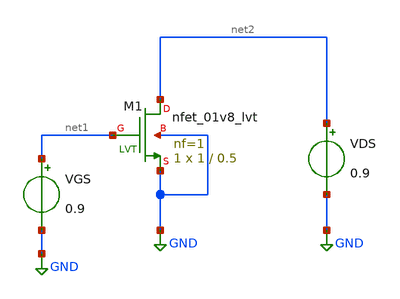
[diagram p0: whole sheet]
** sch_path: Simple-CS-Amplifier/gmid.sch
**.subckt gmid
XM1 net2 net1 GND GND sky130_fd_pr__nfet_01v8_lvt L=0.5 W=1 nf=1 ad='int((nf+1)/2) * W/nf * 0.29' as='int((nf+2)/2) * W/nf * 0.29'
+ pd='2*int((nf+1)/2) * (W/nf + 0.29)' ps='2*int((nf+2)/2) * (W/nf + 0.29)' nrd='0.29 / W' nrs='0.29 / W'
+ sa=0 sb=0 sd=0 mult=1 m=1
VGS net1 GND 0.9
VDS net2 GND 0.9
**** begin user architecture code



.lib /usr/local/share/pdk/sky130A/libs.tech/ngspice/sky130.lib.spice tt
.option wnflag=1 scale=1e-6

.control

save all
save @m.xm1.msky130_fd_pr__nfet_01v8_lvt[id]
save @m.xm1.msky130_fd_pr__nfet_01v8_lvt[gm]
save @m.xm1.msky130_fd_pr__nfet_01v8_lvt[gds]
save @m.xm1.msky130_fd_pr__nfet_01v8_lvt[w]
save @m.xm1.msky130_fd_pr__nfet_01v8_lvt[cgg]
save @m.xm1.msky130_fd_pr__nfet_01v8_lvt[vth]

dc VGS 0 1.8 1m

let id = @m.xm1.msky130_fd_pr__nfet_01v8_lvt[id]
let gm = @m.xm1.msky130_fd_pr__nfet_01v8_lvt[gm]
let ro = 1/@m.xm1.msky130_fd_pr__nfet_01v8_lvt[gds]
let width = @m.xm1.msky130_fd_pr__nfet_01v8_lvt[w]
let cgg = @m.xm1.msky130_fd_pr__nfet_01v8_lvt[cgg]
let vth = @m.xm1.msky130_fd_pr__nfet_01v8_lvt[vth]

let gmoverid = gm/id
let vstar = 2/gmoverid
let gmro = gm*ro
let ft = gm/(2*pi*cgg)

*wrdata charac-L=0.23.txt ft gmro vstar

*meas dc gain find gmro when vstar=0.19
*meas dc freq find ft when vstar=0.19

*meas DC gain FIND gmro WHEN vstar=0.3
*meas DC freq FIND ft WHEN vstar=0.3
*meas DC current FIND id WHEN vstar=0.3

plot gmro



.endc


**** end user architecture code
**.ends
.GLOBAL GND
.end
